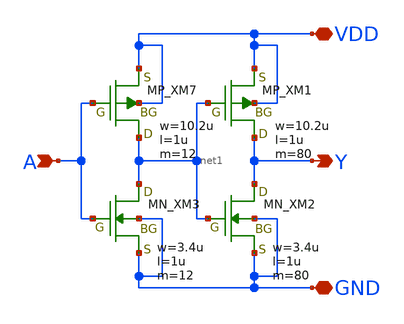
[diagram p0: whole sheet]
** sch_path: openIP62_rev1.0/IP62/Technology/tech/symbols/Xschem/IP62_5_stdcell/CLKBUF_X16.sch
**.subckt CLKBUF_X16 A Y VDD GND
*.ipin A
*.opin Y
*.iopin VDD
*.iopin GND
XM7 net1 A VDD VDD PMOS w=10.2u l=1u as=0 ad=0 ps=0 pd=0 nrd=0 nrs=0 m=12
XM1 Y net1 VDD VDD PMOS w=10.2u l=1u as=0 ad=0 ps=0 pd=0 nrd=0 nrs=0 m=80
XM3 net1 A GND GND NMOS w=3.4u l=1u as=0 ad=0 ps=0 pd=0 nrd=0 nrs=0 m=12
XM2 Y net1 GND GND NMOS w=3.4u l=1u as=0 ad=0 ps=0 pd=0 nrd=0 nrs=0 m=80
**.ends
.end
